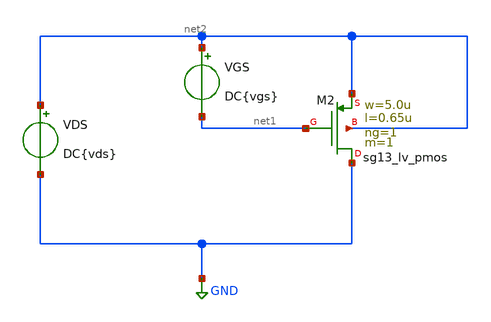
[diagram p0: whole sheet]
** sch_path: design/blocks/tp1_2/schematic/tp1_2.sch
**.subckt tp1_2
VDS net2 GND DC{vds}
XM2 GND net1 net2 net2 sg13_lv_pmos w=5.0u l=0.65u ng=1 m=1 mm_ok=1
VGS net2 net1 DC{vgs}
**** begin user architecture code



* Parameters
.param vds = 1.2
.param vgs = 0.6
.options TEMPS = 27.0

* Include Models
.lib $PDK_ROOT/sg13g2/libs.tech/ngspice/models/sg13_lv_models.lib typical
* Data to save
.save all  @M.XM2.msg13_lv_pmos[id]  @M.XM2.msg13_lv_pmos[gm]  @M.XM2.msg13_lv_pmos[vth]  @M.XM2.msg13_lv_pmos[vds]  @M.XM2.msg13_lv_pmos[vdsat]  @M.XM2.msg13_lv_pmos[vgs]

* Simulation
.control
  dc VDS 0 1.2 0.01 VGS 0 1.2 0.2
  setplot dc1
  plot @M.XM2.msg13_lv_pmos[id] ylabel Id xlabel Vds title 'Id vs Vds vs Vgs'
  set filetype = ascii
  write tp1_2_dc1.raw

  reset
  dc VGS 0 1.2 0.01
  setplot dc2
  plot @M.XM2.msg13_lv_pmos[id] ylabel Id xlabel Vgs
  set filetype = ascii
  write tp1_2_dc2.raw

.endc

.end


**** end user architecture code
**.ends
.GLOBAL GND
.end
